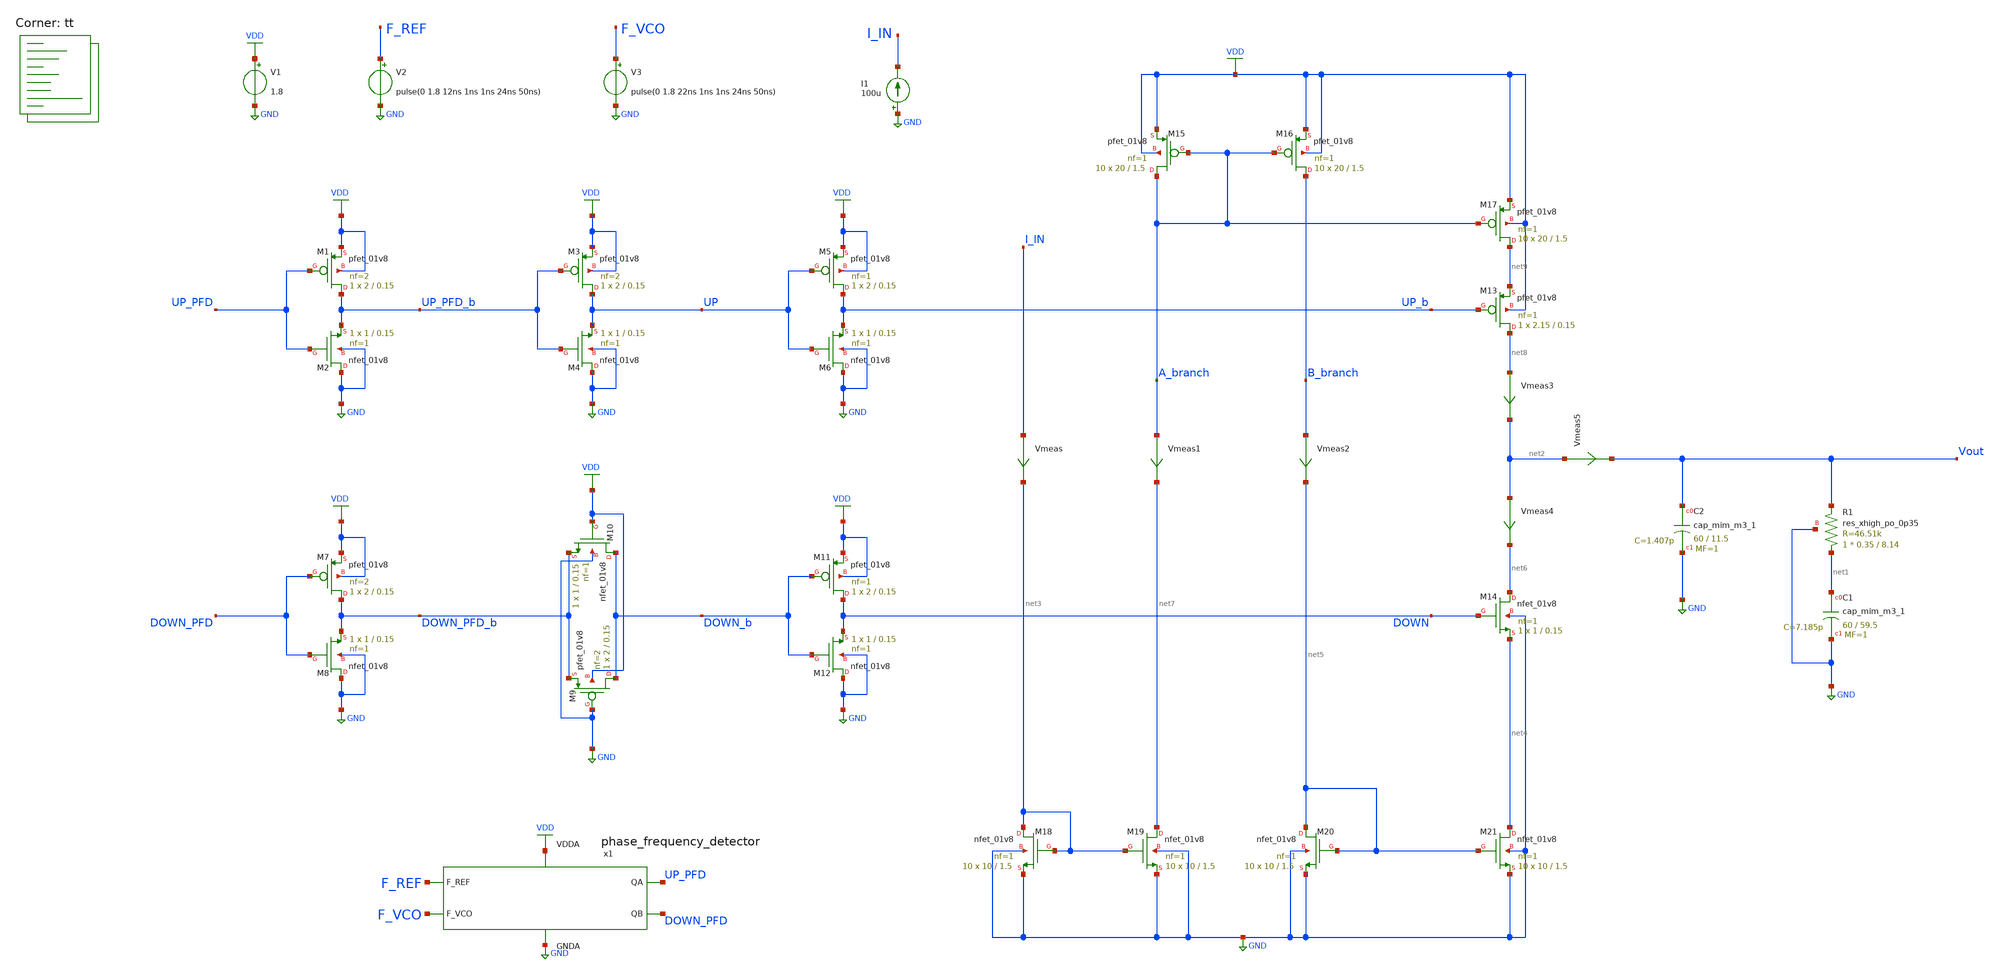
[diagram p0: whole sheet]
** sch_path: projects/pll/charge_pump/xschem_ngspice/pfd_charge_pump_dead_zone_check_2.sch
**.subckt pfd_charge_pump_dead_zone_check_2
V1 VDD GND 1.8
XC2 Vout GND sky130_fd_pr__cap_mim_m3_1 W=60 L=11.5 MF=1 m=1
XC1 net1 GND sky130_fd_pr__cap_mim_m3_1 W=60 L=59.5 MF=1 m=1
V2 F_REF GND pulse(0 1.8 12ns 1ns 1ns 24ns 50ns)
V3 F_VCO GND pulse(0 1.8 22ns 1ns 1ns 24ns 50ns)
x1 F_REF F_VCO VDD UP_PFD DOWN_PFD GND phase_frequency_detector
XR1 net1 Vout GND sky130_fd_pr__res_xhigh_po_0p35 L=8.14 mult=1 m=1
I1 GND I_IN 100u
Vmeas5 net2 Vout 0
.save i(vmeas5)
XM18 net3 net3 GND GND sky130_fd_pr__nfet_01v8 L=1.5 W=10 nf=1 ad='int((nf+1)/2) * W/nf * 0.29' as='int((nf+2)/2) * W/nf * 0.29'
+ pd='2*int((nf+1)/2) * (W/nf + 0.29)' ps='2*int((nf+2)/2) * (W/nf + 0.29)' nrd='0.29 / W' nrs='0.29 / W'
+ sa=0 sb=0 sd=0 mult=10 m=10
XM19 net7 net3 GND GND sky130_fd_pr__nfet_01v8 L=1.5 W=10 nf=1 ad='int((nf+1)/2) * W/nf * 0.29' as='int((nf+2)/2) * W/nf * 0.29'
+ pd='2*int((nf+1)/2) * (W/nf + 0.29)' ps='2*int((nf+2)/2) * (W/nf + 0.29)' nrd='0.29 / W' nrs='0.29 / W'
+ sa=0 sb=0 sd=0 mult=10 m=10
Vmeas I_IN net3 0
.save i(vmeas)
XM13 net8 UP_b net9 VDD sky130_fd_pr__pfet_01v8 L=0.15 W=2.15 nf=1 ad='int((nf+1)/2) * W/nf * 0.29' as='int((nf+2)/2) * W/nf * 0.29'
+ pd='2*int((nf+1)/2) * (W/nf + 0.29)' ps='2*int((nf+2)/2) * (W/nf + 0.29)' nrd='0.29 / W' nrs='0.29 / W'
+ sa=0 sb=0 sd=0 mult=1 m=1
Vmeas3 net8 net2 0
.save i(vmeas3)
Vmeas4 net2 net6 0
.save i(vmeas4)
XM14 net6 DOWN net4 GND sky130_fd_pr__nfet_01v8 L=0.15 W=1 nf=1 ad='int((nf+1)/2) * W/nf * 0.29' as='int((nf+2)/2) * W/nf * 0.29'
+ pd='2*int((nf+1)/2) * (W/nf + 0.29)' ps='2*int((nf+2)/2) * (W/nf + 0.29)' nrd='0.29 / W' nrs='0.29 / W'
+ sa=0 sb=0 sd=0 mult=1 m=1
XM17 net9 A_branch VDD VDD sky130_fd_pr__pfet_01v8 L=1.5 W=20 nf=1 ad='int((nf+1)/2) * W/nf * 0.29' as='int((nf+2)/2) * W/nf * 0.29'
+ pd='2*int((nf+1)/2) * (W/nf + 0.29)' ps='2*int((nf+2)/2) * (W/nf + 0.29)' nrd='0.29 / W' nrs='0.29 / W'
+ sa=0 sb=0 sd=0 mult=10 m=10
XM21 net4 net5 GND GND sky130_fd_pr__nfet_01v8 L=1.5 W=10 nf=1 ad='int((nf+1)/2) * W/nf * 0.29' as='int((nf+2)/2) * W/nf * 0.29'
+ pd='2*int((nf+1)/2) * (W/nf + 0.29)' ps='2*int((nf+2)/2) * (W/nf + 0.29)' nrd='0.29 / W' nrs='0.29 / W'
+ sa=0 sb=0 sd=0 mult=10 m=10
XM20 net5 net5 GND GND sky130_fd_pr__nfet_01v8 L=1.5 W=10 nf=1 ad='int((nf+1)/2) * W/nf * 0.29' as='int((nf+2)/2) * W/nf * 0.29'
+ pd='2*int((nf+1)/2) * (W/nf + 0.29)' ps='2*int((nf+2)/2) * (W/nf + 0.29)' nrd='0.29 / W' nrs='0.29 / W'
+ sa=0 sb=0 sd=0 mult=10 m=10
XM15 A_branch A_branch VDD VDD sky130_fd_pr__pfet_01v8 L=1.5 W=20 nf=1 ad='int((nf+1)/2) * W/nf * 0.29'
+ as='int((nf+2)/2) * W/nf * 0.29' pd='2*int((nf+1)/2) * (W/nf + 0.29)' ps='2*int((nf+2)/2) * (W/nf + 0.29)'
+ nrd='0.29 / W' nrs='0.29 / W' sa=0 sb=0 sd=0 mult=10 m=10
XM16 B_branch A_branch VDD VDD sky130_fd_pr__pfet_01v8 L=1.5 W=20 nf=1 ad='int((nf+1)/2) * W/nf * 0.29'
+ as='int((nf+2)/2) * W/nf * 0.29' pd='2*int((nf+1)/2) * (W/nf + 0.29)' ps='2*int((nf+2)/2) * (W/nf + 0.29)'
+ nrd='0.29 / W' nrs='0.29 / W' sa=0 sb=0 sd=0 mult=10 m=10
Vmeas1 A_branch net7 0
.save i(vmeas1)
Vmeas2 B_branch net5 0
.save i(vmeas2)
XM9 DOWN_b GND DOWN_PFD_b VDD sky130_fd_pr__pfet_01v8 L=0.15 W=2 nf=2 ad='int((nf+1)/2) * W/nf * 0.29'
+ as='int((nf+2)/2) * W/nf * 0.29' pd='2*int((nf+1)/2) * (W/nf + 0.29)' ps='2*int((nf+2)/2) * (W/nf + 0.29)'
+ nrd='0.29 / W' nrs='0.29 / W' sa=0 sb=0 sd=0 mult=1 m=1
XM10 DOWN_b VDD DOWN_PFD_b GND sky130_fd_pr__nfet_01v8 L=0.15 W=1 nf=1 ad='int((nf+1)/2) * W/nf * 0.29'
+ as='int((nf+2)/2) * W/nf * 0.29' pd='2*int((nf+1)/2) * (W/nf + 0.29)' ps='2*int((nf+2)/2) * (W/nf + 0.29)'
+ nrd='0.29 / W' nrs='0.29 / W' sa=0 sb=0 sd=0 mult=1 m=1
XM1 UP_PFD_b UP_PFD VDD VDD sky130_fd_pr__pfet_01v8 L=0.15 W=2 nf=2 ad='int((nf+1)/2) * W/nf * 0.29'
+ as='int((nf+2)/2) * W/nf * 0.29' pd='2*int((nf+1)/2) * (W/nf + 0.29)' ps='2*int((nf+2)/2) * (W/nf + 0.29)'
+ nrd='0.29 / W' nrs='0.29 / W' sa=0 sb=0 sd=0 mult=1 m=1
XM2 GND UP_PFD UP_PFD_b GND sky130_fd_pr__nfet_01v8 L=0.15 W=1 nf=1 ad='int((nf+1)/2) * W/nf * 0.29'
+ as='int((nf+2)/2) * W/nf * 0.29' pd='2*int((nf+1)/2) * (W/nf + 0.29)' ps='2*int((nf+2)/2) * (W/nf + 0.29)'
+ nrd='0.29 / W' nrs='0.29 / W' sa=0 sb=0 sd=0 mult=1 m=1
XM7 DOWN_PFD_b DOWN_PFD VDD VDD sky130_fd_pr__pfet_01v8 L=0.15 W=2 nf=2 ad='int((nf+1)/2) * W/nf * 0.29'
+ as='int((nf+2)/2) * W/nf * 0.29' pd='2*int((nf+1)/2) * (W/nf + 0.29)' ps='2*int((nf+2)/2) * (W/nf + 0.29)'
+ nrd='0.29 / W' nrs='0.29 / W' sa=0 sb=0 sd=0 mult=1 m=1
XM8 GND DOWN_PFD DOWN_PFD_b GND sky130_fd_pr__nfet_01v8 L=0.15 W=1 nf=1 ad='int((nf+1)/2) * W/nf * 0.29'
+ as='int((nf+2)/2) * W/nf * 0.29' pd='2*int((nf+1)/2) * (W/nf + 0.29)' ps='2*int((nf+2)/2) * (W/nf + 0.29)'
+ nrd='0.29 / W' nrs='0.29 / W' sa=0 sb=0 sd=0 mult=1 m=1
XM3 UP UP_PFD_b VDD VDD sky130_fd_pr__pfet_01v8 L=0.15 W=2 nf=2 ad='int((nf+1)/2) * W/nf * 0.29' as='int((nf+2)/2) * W/nf * 0.29'
+ pd='2*int((nf+1)/2) * (W/nf + 0.29)' ps='2*int((nf+2)/2) * (W/nf + 0.29)' nrd='0.29 / W' nrs='0.29 / W'
+ sa=0 sb=0 sd=0 mult=1 m=1
XM4 GND UP_PFD_b UP GND sky130_fd_pr__nfet_01v8 L=0.15 W=1 nf=1 ad='int((nf+1)/2) * W/nf * 0.29' as='int((nf+2)/2) * W/nf * 0.29'
+ pd='2*int((nf+1)/2) * (W/nf + 0.29)' ps='2*int((nf+2)/2) * (W/nf + 0.29)' nrd='0.29 / W' nrs='0.29 / W'
+ sa=0 sb=0 sd=0 mult=1 m=1
XM5 UP_b UP VDD VDD sky130_fd_pr__pfet_01v8 L=0.15 W=2 nf=1 ad='int((nf+1)/2) * W/nf * 0.29' as='int((nf+2)/2) * W/nf * 0.29'
+ pd='2*int((nf+1)/2) * (W/nf + 0.29)' ps='2*int((nf+2)/2) * (W/nf + 0.29)' nrd='0.29 / W' nrs='0.29 / W'
+ sa=0 sb=0 sd=0 mult=1 m=1
XM6 GND UP UP_b GND sky130_fd_pr__nfet_01v8 L=0.15 W=1 nf=1 ad='int((nf+1)/2) * W/nf * 0.29' as='int((nf+2)/2) * W/nf * 0.29'
+ pd='2*int((nf+1)/2) * (W/nf + 0.29)' ps='2*int((nf+2)/2) * (W/nf + 0.29)' nrd='0.29 / W' nrs='0.29 / W'
+ sa=0 sb=0 sd=0 mult=1 m=1
XM11 DOWN DOWN_b VDD VDD sky130_fd_pr__pfet_01v8 L=0.15 W=2 nf=1 ad='int((nf+1)/2) * W/nf * 0.29' as='int((nf+2)/2) * W/nf * 0.29'
+ pd='2*int((nf+1)/2) * (W/nf + 0.29)' ps='2*int((nf+2)/2) * (W/nf + 0.29)' nrd='0.29 / W' nrs='0.29 / W'
+ sa=0 sb=0 sd=0 mult=1 m=1
XM12 GND DOWN_b DOWN GND sky130_fd_pr__nfet_01v8 L=0.15 W=1 nf=1 ad='int((nf+1)/2) * W/nf * 0.29' as='int((nf+2)/2) * W/nf * 0.29'
+ pd='2*int((nf+1)/2) * (W/nf + 0.29)' ps='2*int((nf+2)/2) * (W/nf + 0.29)' nrd='0.29 / W' nrs='0.29 / W'
+ sa=0 sb=0 sd=0 mult=1 m=1
**** begin user architecture code
.lib $::SKYWATER_MODELS/sky130.lib.spice tt



**** end user architecture code
**.ends
.GLOBAL GND
.GLOBAL VDD
.end
